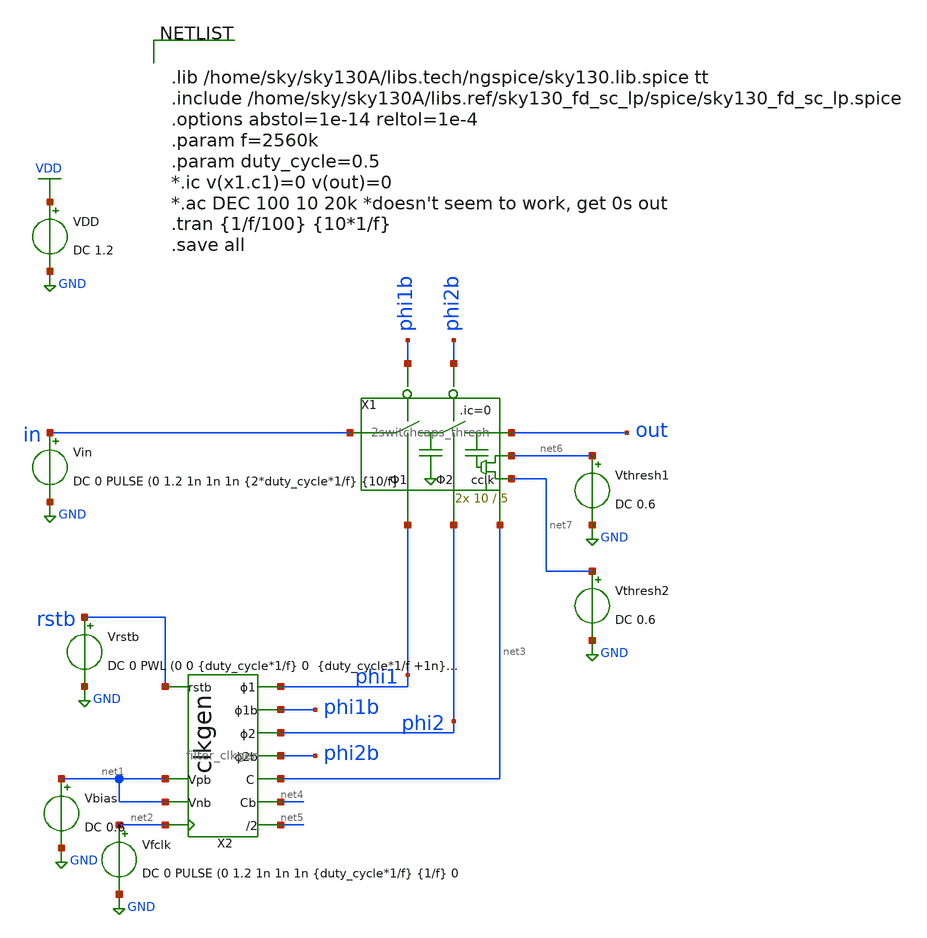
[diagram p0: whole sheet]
** sch_path: xschem/Switched_Caps/2switchcaps_thresh_tb.sch
**.subckt 2switchcaps_thresh_tb
Vin in GND DC 0 PULSE (0 1.2 1n 1n 1n {2*duty_cycle*1/f} {10/f}
VDD VDD GND DC 1.2
Vfclk net2 GND DC 0 PULSE (0 1.2 1n 1n 1n {duty_cycle*1/f} {1/f} 0
X1 in out phi2 phi1 phi1b phi2b net7 net3 net6 2switchcaps_thresh Wcap=10 Lcap=5
X2 rstb net2 phi2b phi2 phi1b phi1 net4 net3 net5 net1 net1 filter_clkgen
Vbias net1 GND DC 0.6
Vthresh1 net6 GND DC 0.6
Vthresh2 net7 GND DC 0.6
Vrstb rstb GND DC 0 PWL (0 0 {duty_cycle*1/f} 0 {duty_cycle*1/f +1n} 1.2}
**** begin user architecture code


.lib /home/sky/sky130A/libs.tech/ngspice/sky130.lib.spice tt
.include /home/sky/sky130A/libs.ref/sky130_fd_sc_lp/spice/sky130_fd_sc_lp.spice
.options abstol=1e-14 reltol=1e-4
.param f=2560k
.param duty_cycle=0.5
*.ic v(x1.c1)=0 v(out)=0
*.ac DEC 100 10 20k *doesn't seem to work, get 0s out
.tran {1/f/100} {10*1/f}
.save all


**** end user architecture code
**.ends
.GLOBAL GND
.GLOBAL VDD
.end
